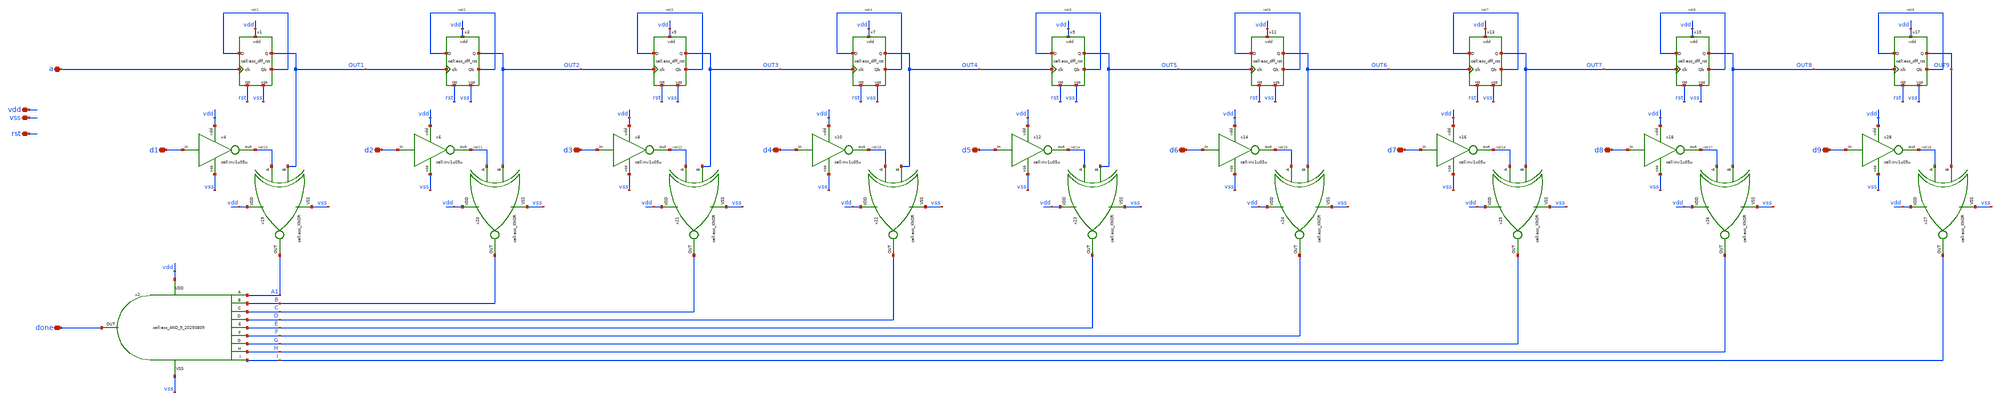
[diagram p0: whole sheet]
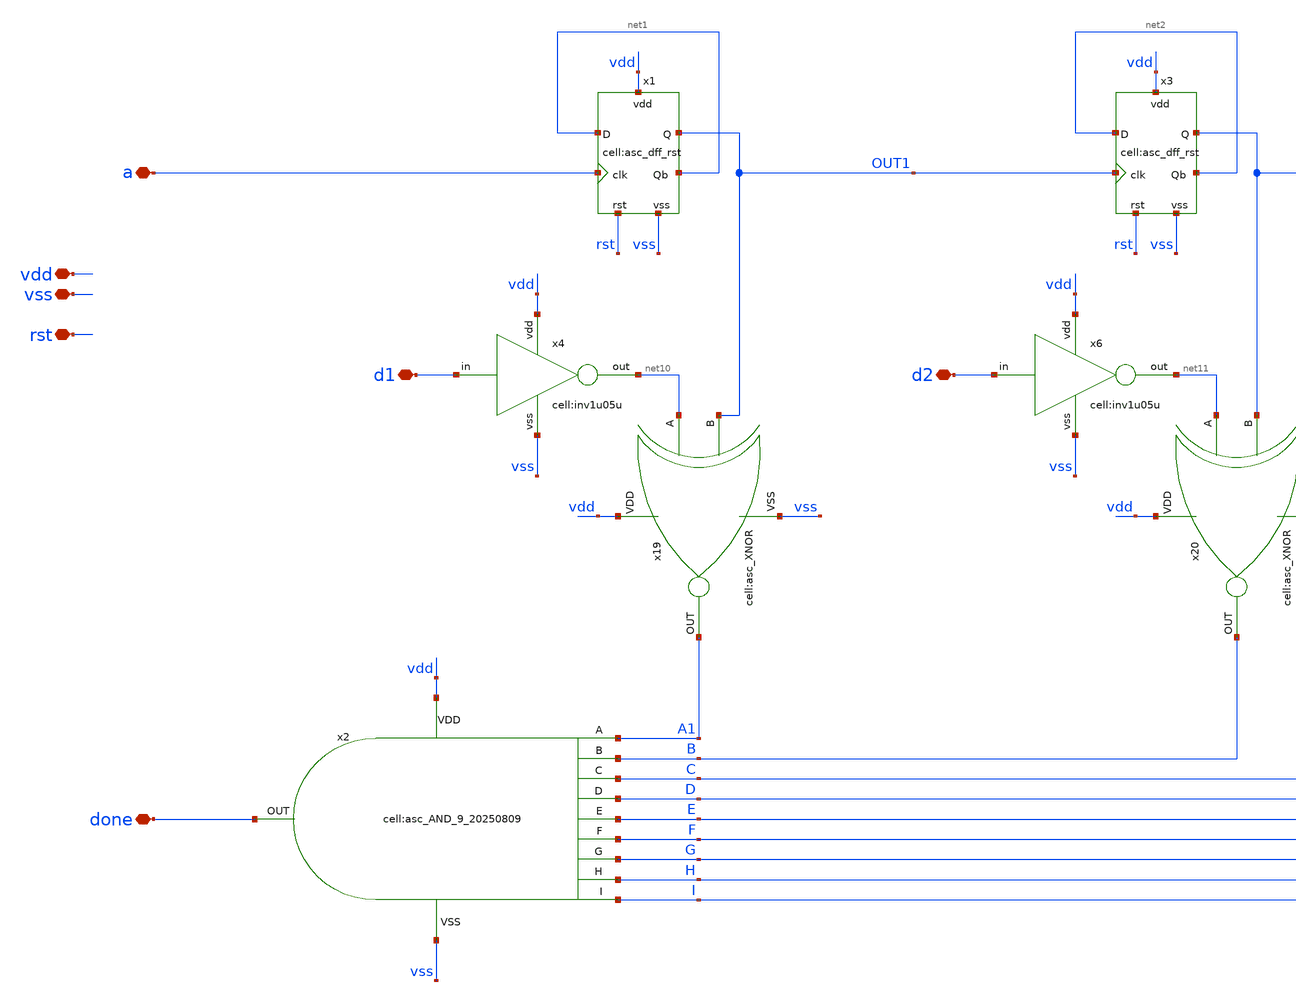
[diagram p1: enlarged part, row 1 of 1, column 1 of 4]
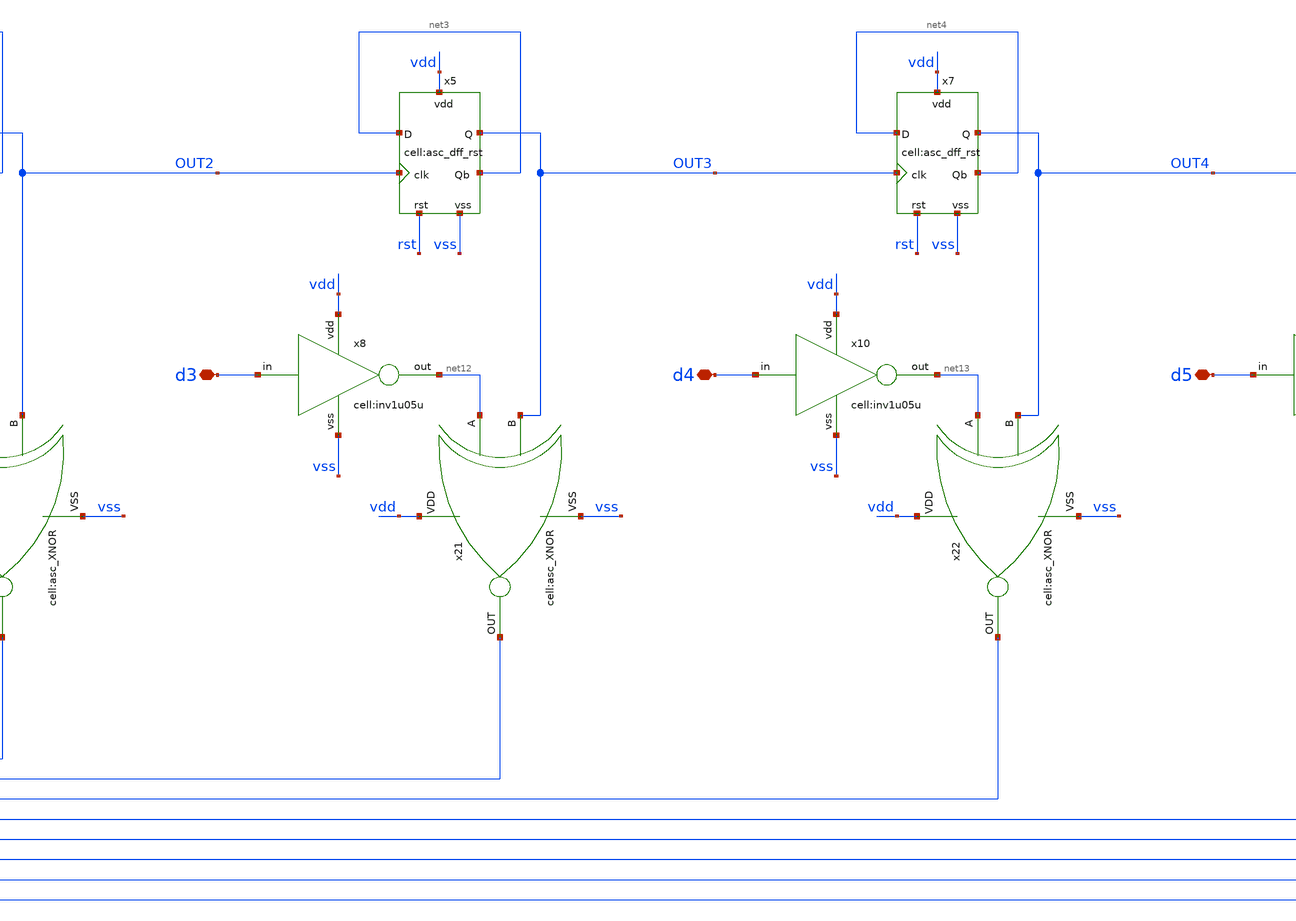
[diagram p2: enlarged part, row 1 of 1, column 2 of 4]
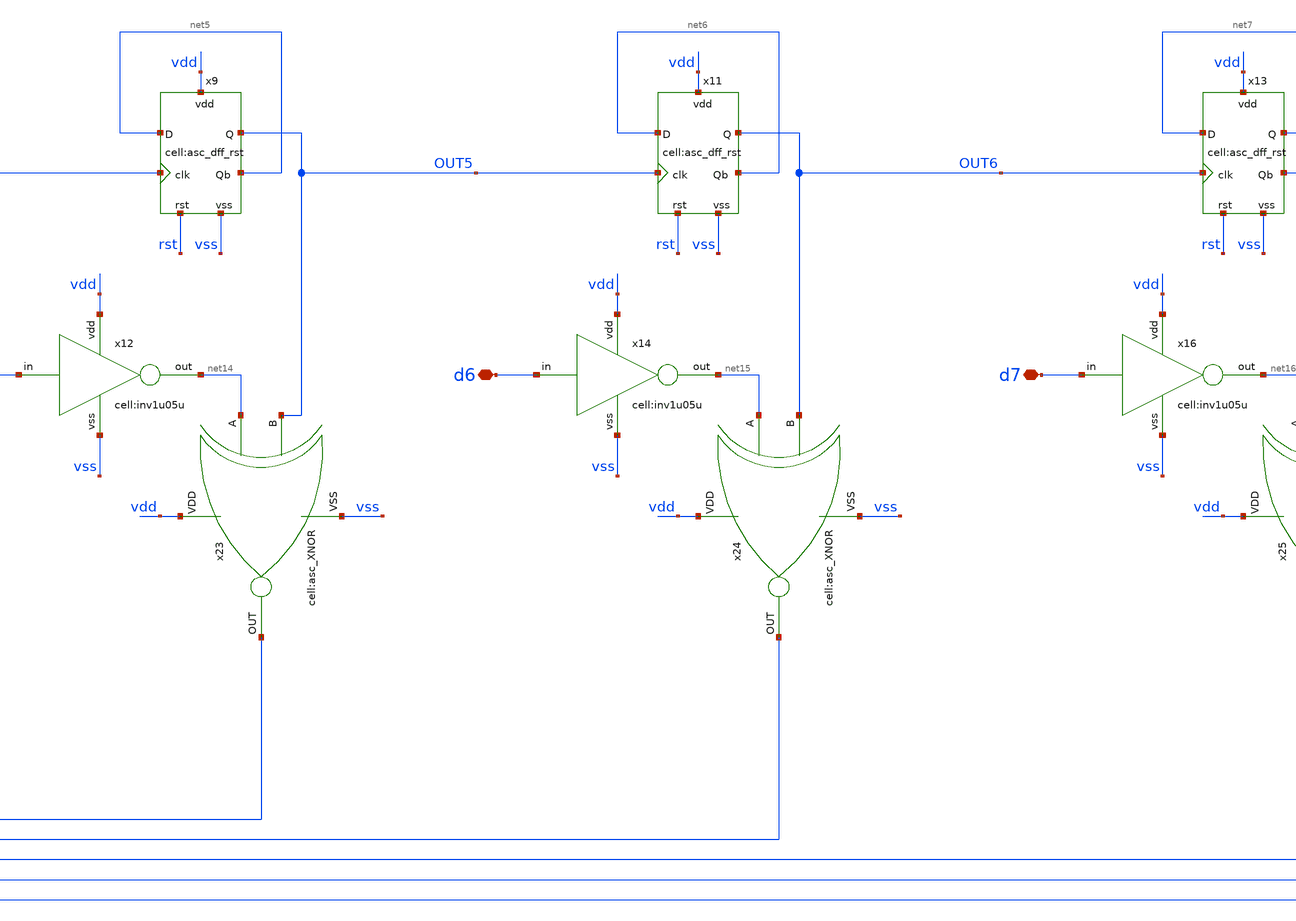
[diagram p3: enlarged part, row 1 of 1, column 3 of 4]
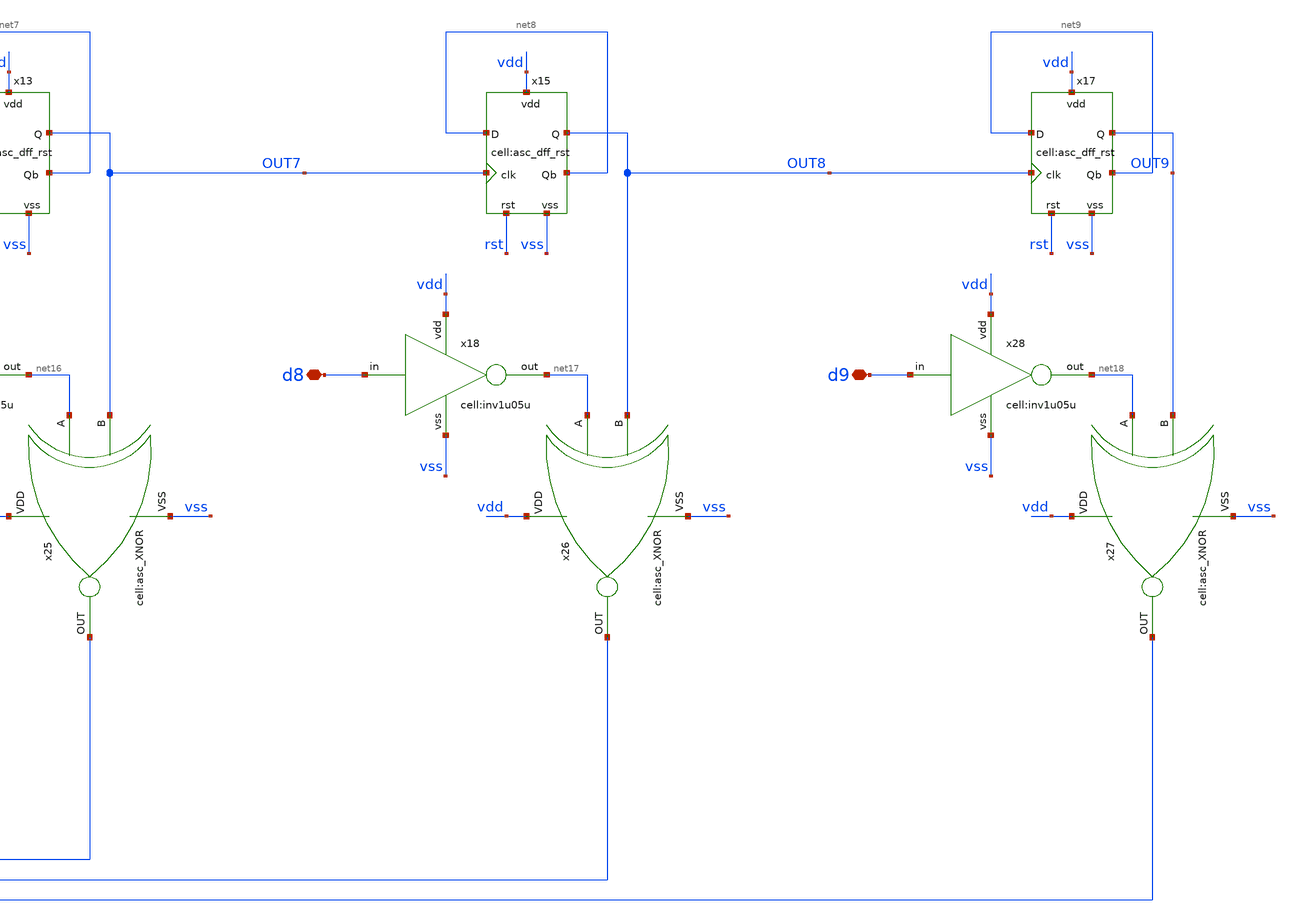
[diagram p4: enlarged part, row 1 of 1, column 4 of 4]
** sch_path: designs/libs/core_analog/asc_9_bit_counter_20250809/asc_9_bit_counter_20250809.sch
**.subckt asc_9_bit_counter_20250809 a vdd vss done d1 d2 d3 d4 d5 d6 d7 d8 d9 rst
*.iopin a
*.iopin vdd
*.iopin vss
*.iopin done
*.iopin d1
*.iopin d2
*.iopin d3
*.iopin d4
*.iopin d5
*.iopin d6
*.iopin d7
*.iopin d8
*.iopin d9
*.iopin rst
x19 vdd vss A1 net10 OUT1 asc_XNOR
x20 vdd vss B net11 OUT2 asc_XNOR
x21 vdd vss C net12 OUT3 asc_XNOR
x22 vdd vss D net13 OUT4 asc_XNOR
x23 vdd vss E net14 OUT5 asc_XNOR
x24 vdd vss F net15 OUT6 asc_XNOR
x25 vdd vss G net16 OUT7 asc_XNOR
x26 vdd vss H net17 OUT8 asc_XNOR
x27 vdd vss I net18 OUT9 asc_XNOR
x1 a net1 net1 vdd vss OUT1 rst asc_dff_rst
x3 OUT1 net2 net2 vdd vss OUT2 rst asc_dff_rst
x5 OUT2 net3 net3 vdd vss OUT3 rst asc_dff_rst
x7 OUT3 net4 net4 vdd vss OUT4 rst asc_dff_rst
x9 OUT4 net5 net5 vdd vss OUT5 rst asc_dff_rst
x11 OUT5 net6 net6 vdd vss OUT6 rst asc_dff_rst
x13 OUT6 net7 net7 vdd vss OUT7 rst asc_dff_rst
x15 OUT7 net8 net8 vdd vss OUT8 rst asc_dff_rst
x17 OUT8 net9 net9 vdd vss OUT9 rst asc_dff_rst
x2 vdd vss done A1 B C D E F G H I asc_AND_9_20250809
x4 d1 vdd net10 vss inv1u05u
x6 d2 vdd net11 vss inv1u05u
x8 d3 vdd net12 vss inv1u05u
x10 d4 vdd net13 vss inv1u05u
x12 d5 vdd net14 vss inv1u05u
x14 d6 vdd net15 vss inv1u05u
x16 d7 vdd net16 vss inv1u05u
x18 d8 vdd net17 vss inv1u05u
x28 d9 vdd net18 vss inv1u05u
**.ends
.end
